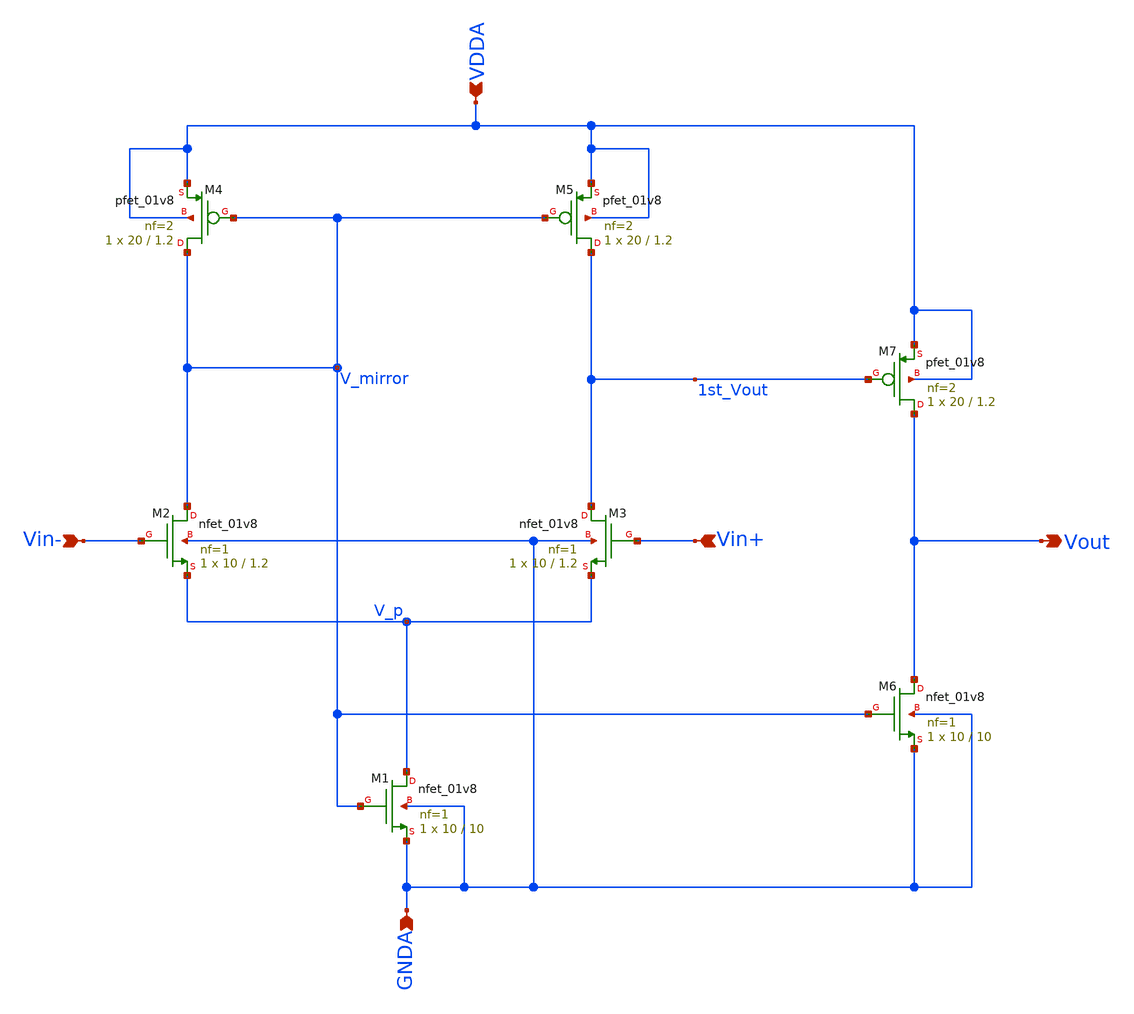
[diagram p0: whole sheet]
** sch_path: projects/bandgapref/xschem_ngspice/new_files/opamp_bandgap_2.sch
**.subckt opamp_bandgap_2 Vin+ Vout Vin- GNDA VDDA
*.ipin Vin+
*.opin Vout
*.ipin Vin-
*.ipin GNDA
*.ipin VDDA
XM1 V_p V_mirror GNDA GNDA sky130_fd_pr__nfet_01v8 L=10 W=10 nf=1 ad='int((nf+1)/2) * W/nf * 0.29' as='int((nf+2)/2) * W/nf * 0.29'
+ pd='2*int((nf+1)/2) * (W/nf + 0.29)' ps='2*int((nf+2)/2) * (W/nf + 0.29)' nrd='0.29 / W' nrs='0.29 / W'
+ sa=0 sb=0 sd=0 mult=1 m=1
XM2 V_mirror Vin- V_p GNDA sky130_fd_pr__nfet_01v8 L=1.2 W=10 nf=1 ad='int((nf+1)/2) * W/nf * 0.29' as='int((nf+2)/2) * W/nf * 0.29'
+ pd='2*int((nf+1)/2) * (W/nf + 0.29)' ps='2*int((nf+2)/2) * (W/nf + 0.29)' nrd='0.29 / W' nrs='0.29 / W'
+ sa=0 sb=0 sd=0 mult=1 m=1
XM3 1st_Vout Vin+ V_p GNDA sky130_fd_pr__nfet_01v8 L=1.2 W=10 nf=1 ad='int((nf+1)/2) * W/nf * 0.29' as='int((nf+2)/2) * W/nf * 0.29'
+ pd='2*int((nf+1)/2) * (W/nf + 0.29)' ps='2*int((nf+2)/2) * (W/nf + 0.29)' nrd='0.29 / W' nrs='0.29 / W'
+ sa=0 sb=0 sd=0 mult=1 m=1
XM4 V_mirror V_mirror VDDA VDDA sky130_fd_pr__pfet_01v8 L=1.2 W=20 nf=2 ad='int((nf+1)/2) * W/nf * 0.29'
+ as='int((nf+2)/2) * W/nf * 0.29' pd='2*int((nf+1)/2) * (W/nf + 0.29)' ps='2*int((nf+2)/2) * (W/nf + 0.29)'
+ nrd='0.29 / W' nrs='0.29 / W' sa=0 sb=0 sd=0 mult=1 m=1
XM5 1st_Vout V_mirror VDDA VDDA sky130_fd_pr__pfet_01v8 L=1.2 W=20 nf=2 ad='int((nf+1)/2) * W/nf * 0.29'
+ as='int((nf+2)/2) * W/nf * 0.29' pd='2*int((nf+1)/2) * (W/nf + 0.29)' ps='2*int((nf+2)/2) * (W/nf + 0.29)'
+ nrd='0.29 / W' nrs='0.29 / W' sa=0 sb=0 sd=0 mult=1 m=1
XM6 Vout V_mirror GNDA GNDA sky130_fd_pr__nfet_01v8 L=10 W=10 nf=1 ad='int((nf+1)/2) * W/nf * 0.29' as='int((nf+2)/2) * W/nf * 0.29'
+ pd='2*int((nf+1)/2) * (W/nf + 0.29)' ps='2*int((nf+2)/2) * (W/nf + 0.29)' nrd='0.29 / W' nrs='0.29 / W'
+ sa=0 sb=0 sd=0 mult=1 m=1
XM7 Vout 1st_Vout VDDA VDDA sky130_fd_pr__pfet_01v8 L=1.2 W=20 nf=2 ad='int((nf+1)/2) * W/nf * 0.29'
+ as='int((nf+2)/2) * W/nf * 0.29' pd='2*int((nf+1)/2) * (W/nf + 0.29)' ps='2*int((nf+2)/2) * (W/nf + 0.29)'
+ nrd='0.29 / W' nrs='0.29 / W' sa=0 sb=0 sd=0 mult=1 m=1
**.ends
.end
